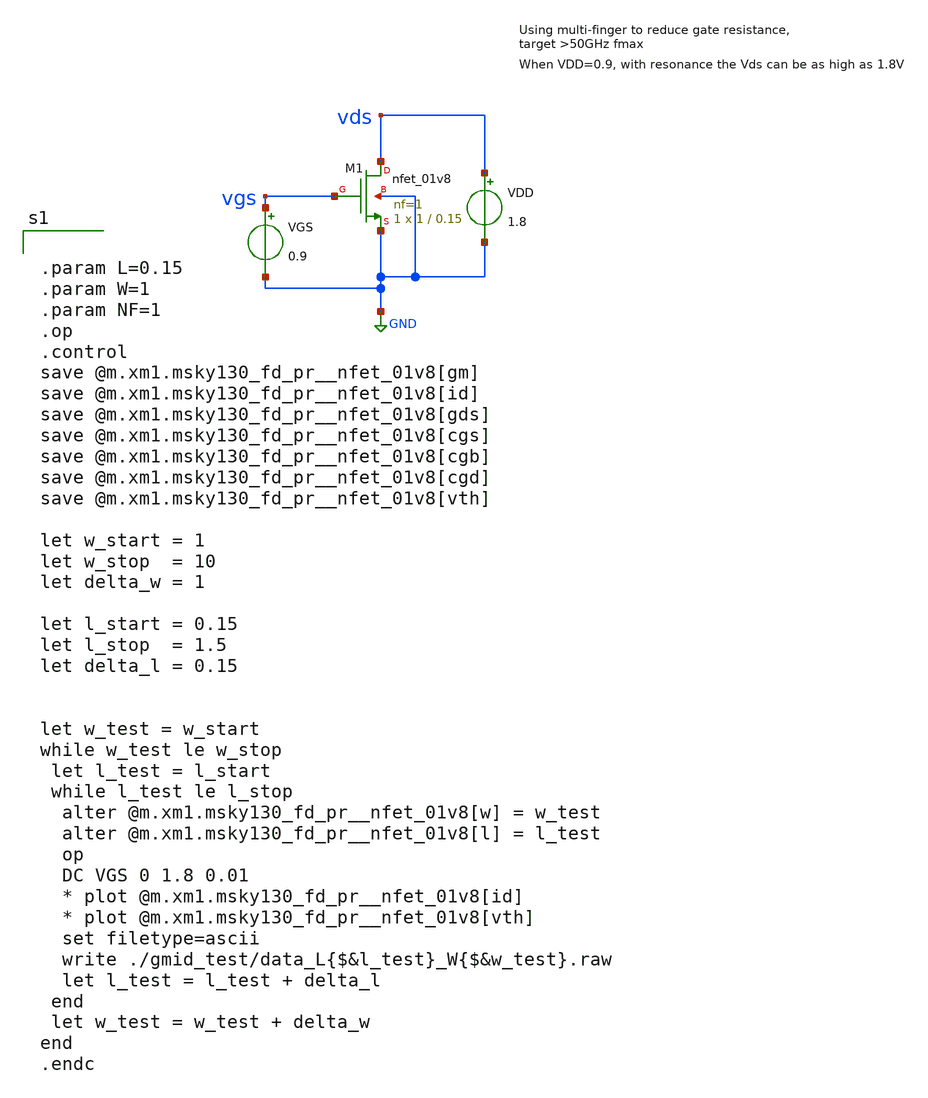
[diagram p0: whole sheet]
** sch_path: xschem/gmid_test/nmos_test.sch
**.subckt nmos_test
XM1 vds vgs GND GND sky130_fd_pr__nfet_01v8 L=0.15 W=1 nf=1 ad='int((nf+1)/2) * W * 0.29' as='int((nf+2)/2) * W * 0.29'
+ pd='2*int((nf+1)/2) * (W + 0.29)' ps='2*int((nf+2)/2) * (W + 0.29)' nrd='0.29 / W / nf' nrs='0.29 / W / nf'
+ sa=0 sb=0 sd=0 mult=1 m=1
VGS vgs GND 0.9
VDD vds GND 1.8
**** begin user architecture code


.param L=0.15
.param W=1
.param NF=1
.op
.control
save @m.xm1.msky130_fd_pr__nfet_01v8[gm]
save @m.xm1.msky130_fd_pr__nfet_01v8[id]
save @m.xm1.msky130_fd_pr__nfet_01v8[gds]
save @m.xm1.msky130_fd_pr__nfet_01v8[cgs]
save @m.xm1.msky130_fd_pr__nfet_01v8[cgb]
save @m.xm1.msky130_fd_pr__nfet_01v8[cgd]
save @m.xm1.msky130_fd_pr__nfet_01v8[vth]

let w_start = 1
let w_stop  = 10
let delta_w = 1

let l_start = 0.15
let l_stop  = 1.5
let delta_l = 0.15


let w_test = w_start
while w_test le w_stop
 let l_test = l_start
 while l_test le l_stop
  alter @m.xm1.msky130_fd_pr__nfet_01v8[w] = w_test
  alter @m.xm1.msky130_fd_pr__nfet_01v8[l] = l_test
  op
  DC VGS 0 1.8 0.01
  * plot @m.xm1.msky130_fd_pr__nfet_01v8[id]
  * plot @m.xm1.msky130_fd_pr__nfet_01v8[vth]
  set filetype=ascii
  write ./gmid_test/data_L{$&l_test}_W{$&w_test}.raw
  let l_test = l_test + delta_l
 end
 let w_test = w_test + delta_w
end
.endc


.lib $::SKYWATER_MODELS/sky130.lib.spice tt
.include $::PDKPATH/libs.ref/sky130_fd_sc_hvl/spice/sky130_fd_sc_hvl.spice
**** end user architecture code
**.ends
.GLOBAL GND
.end
